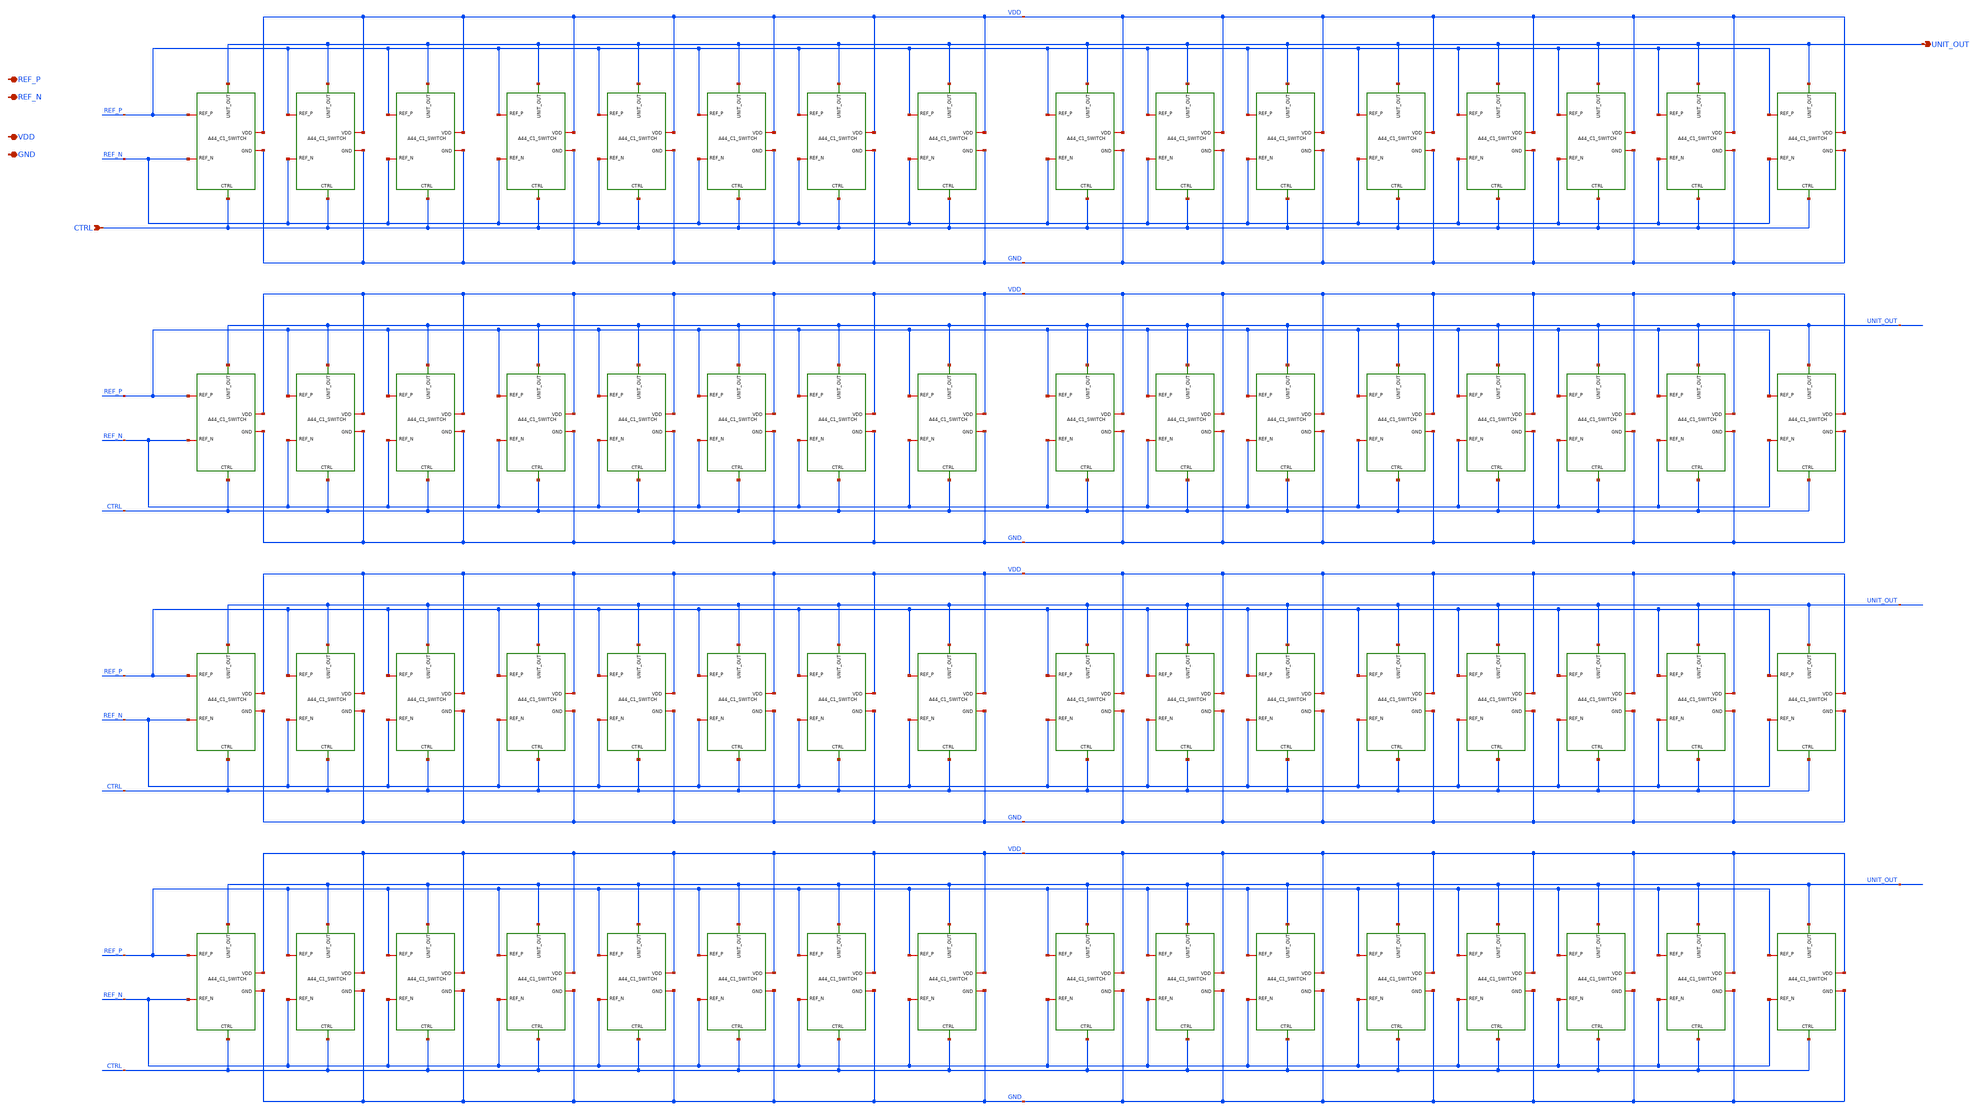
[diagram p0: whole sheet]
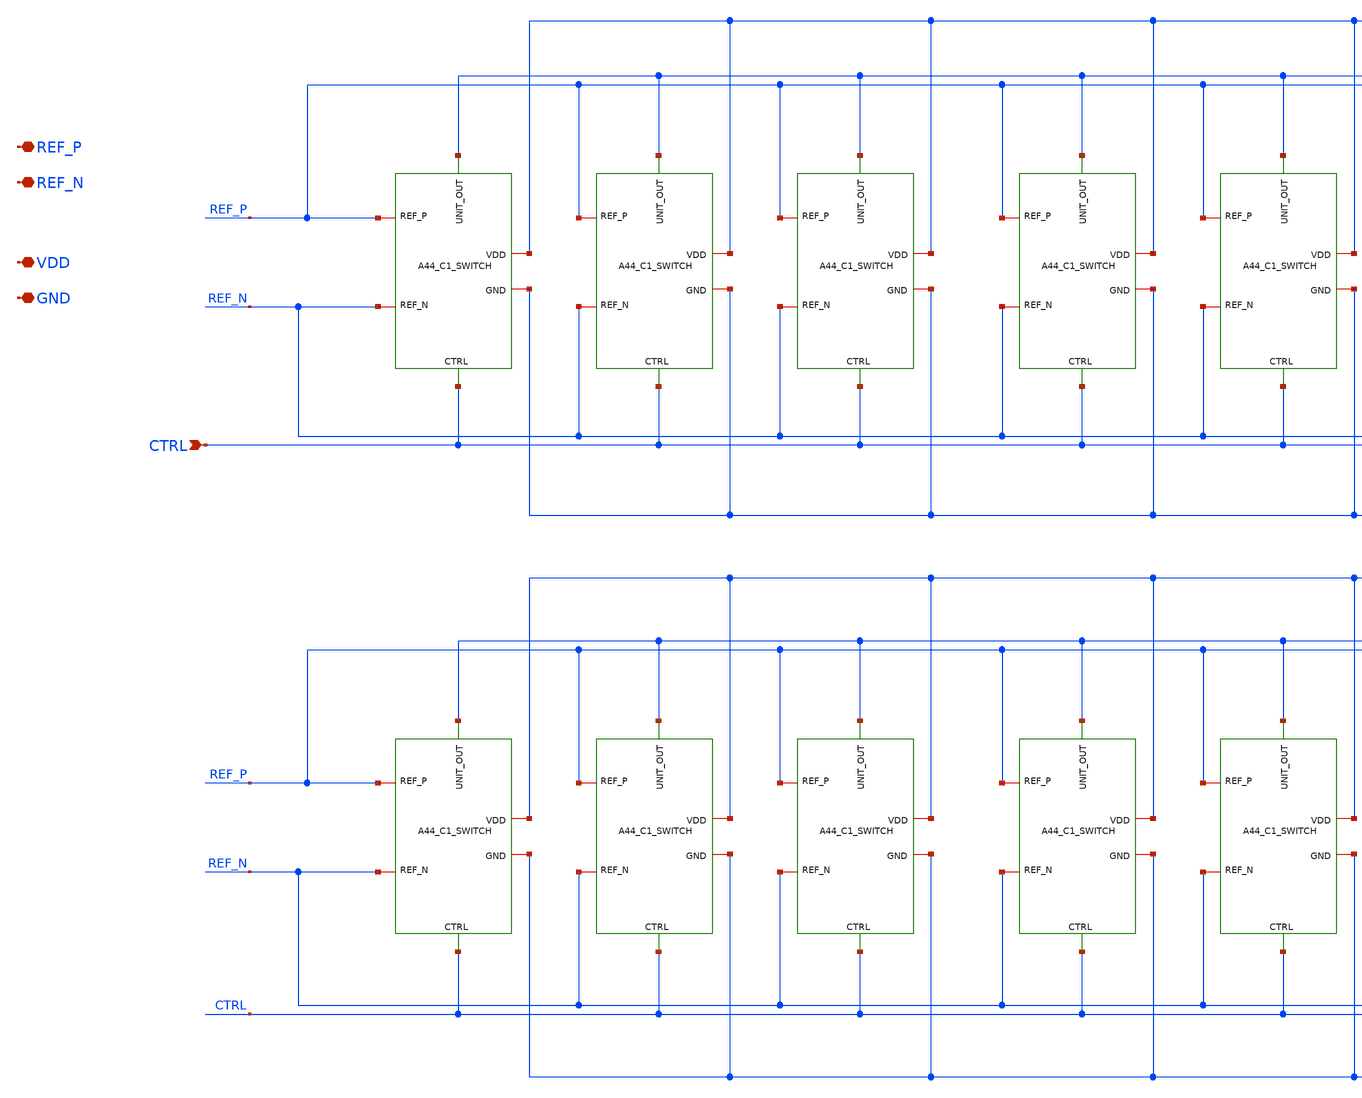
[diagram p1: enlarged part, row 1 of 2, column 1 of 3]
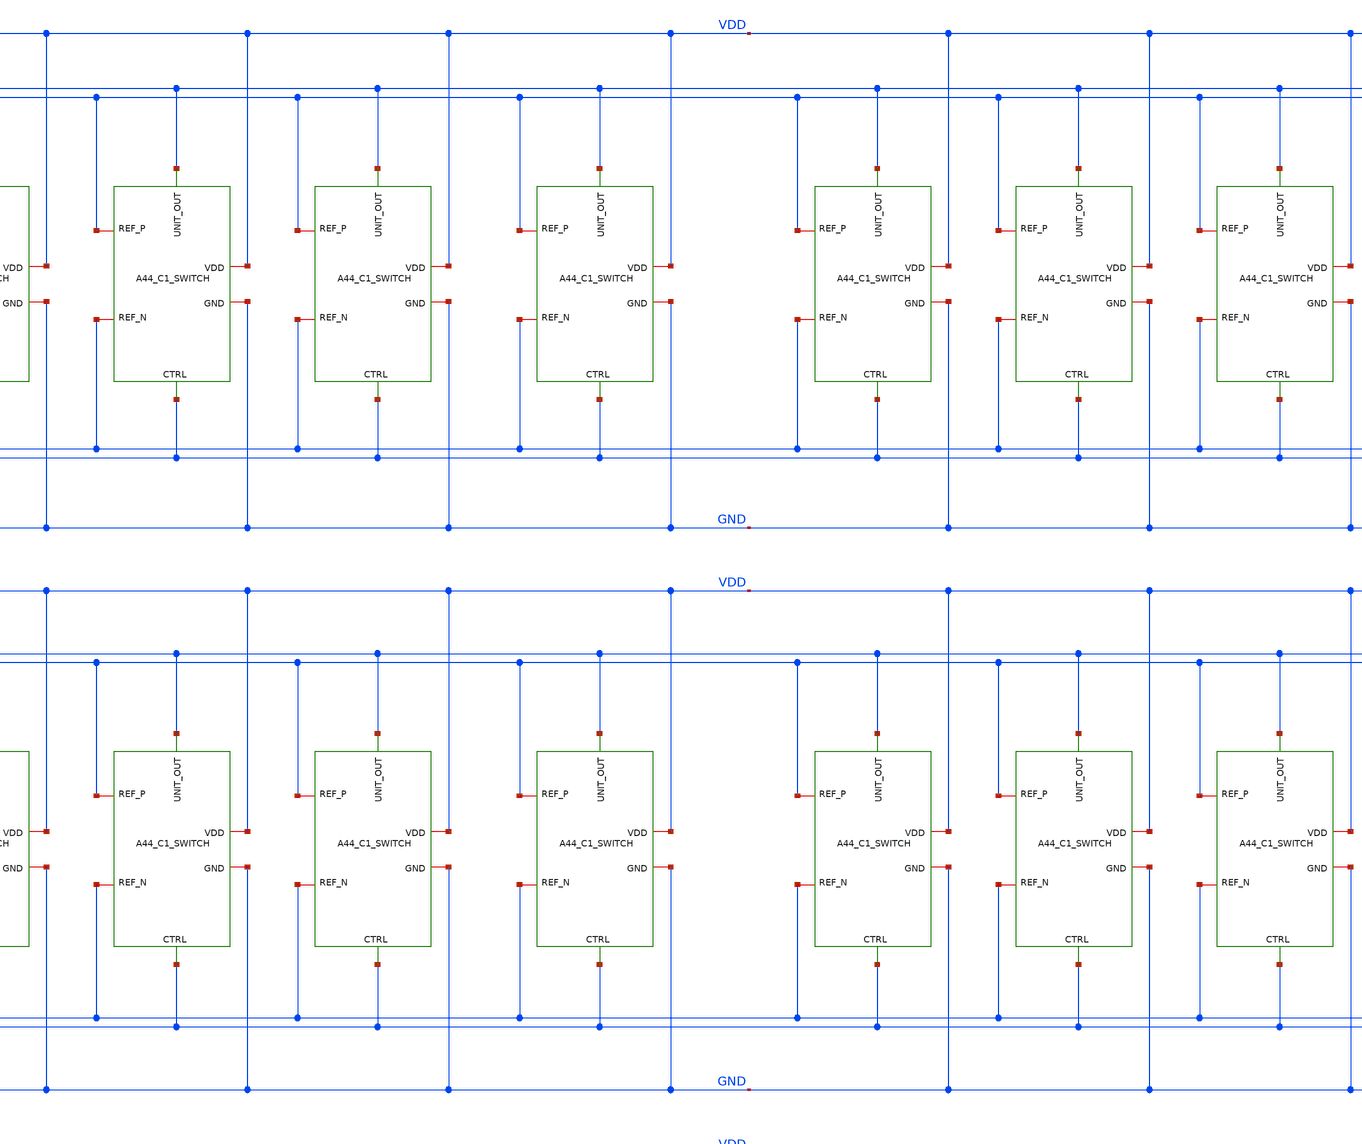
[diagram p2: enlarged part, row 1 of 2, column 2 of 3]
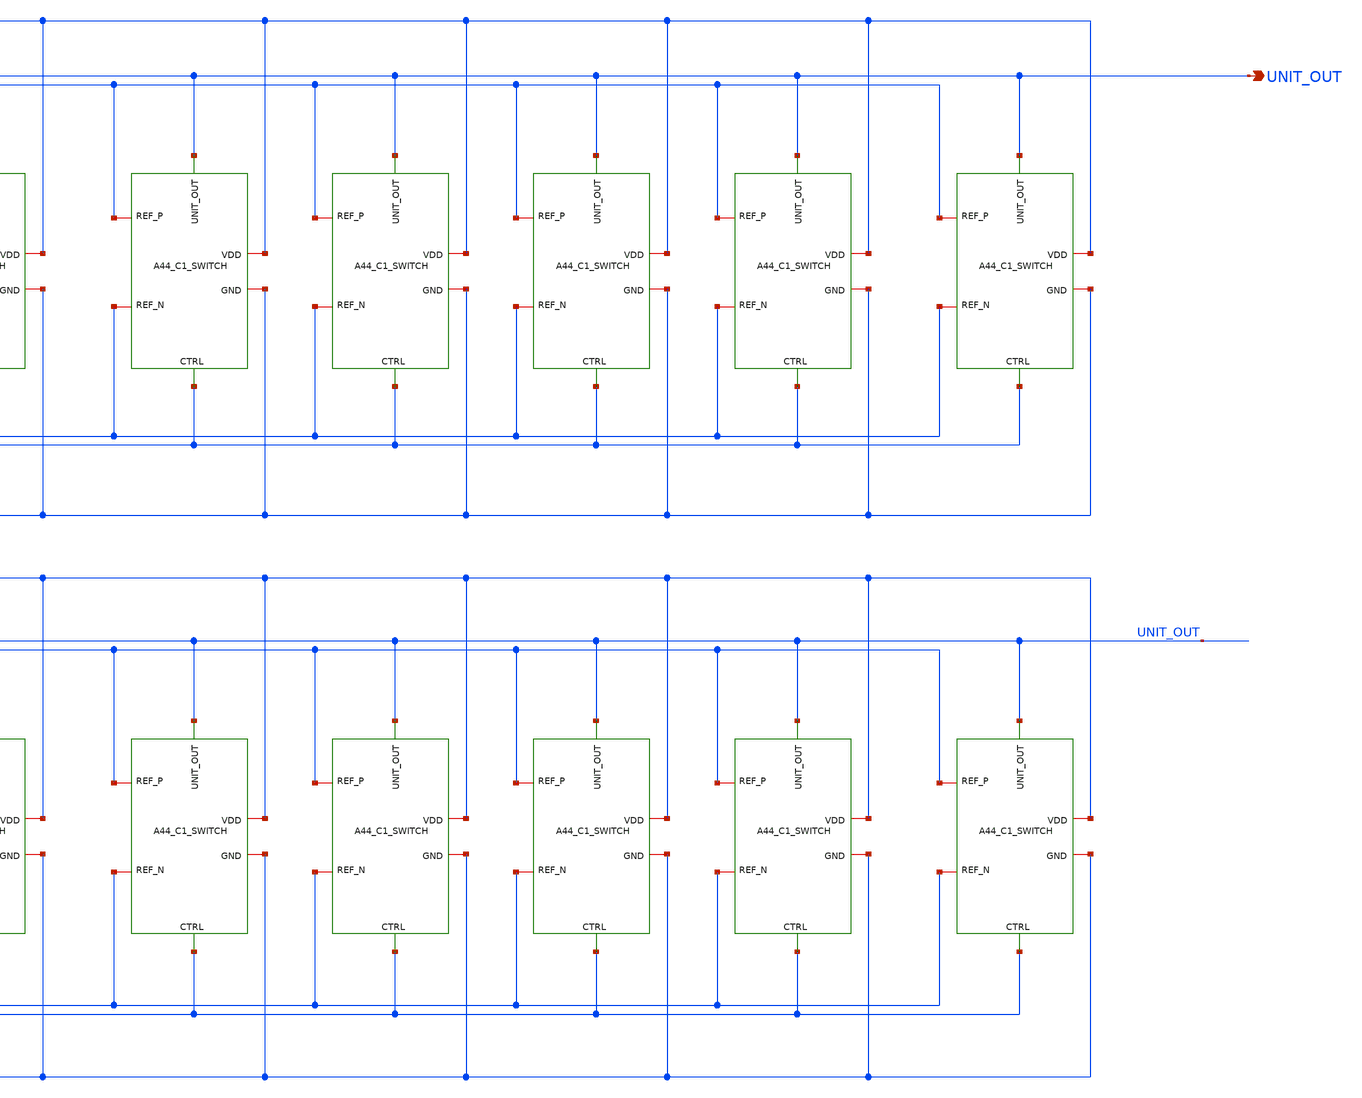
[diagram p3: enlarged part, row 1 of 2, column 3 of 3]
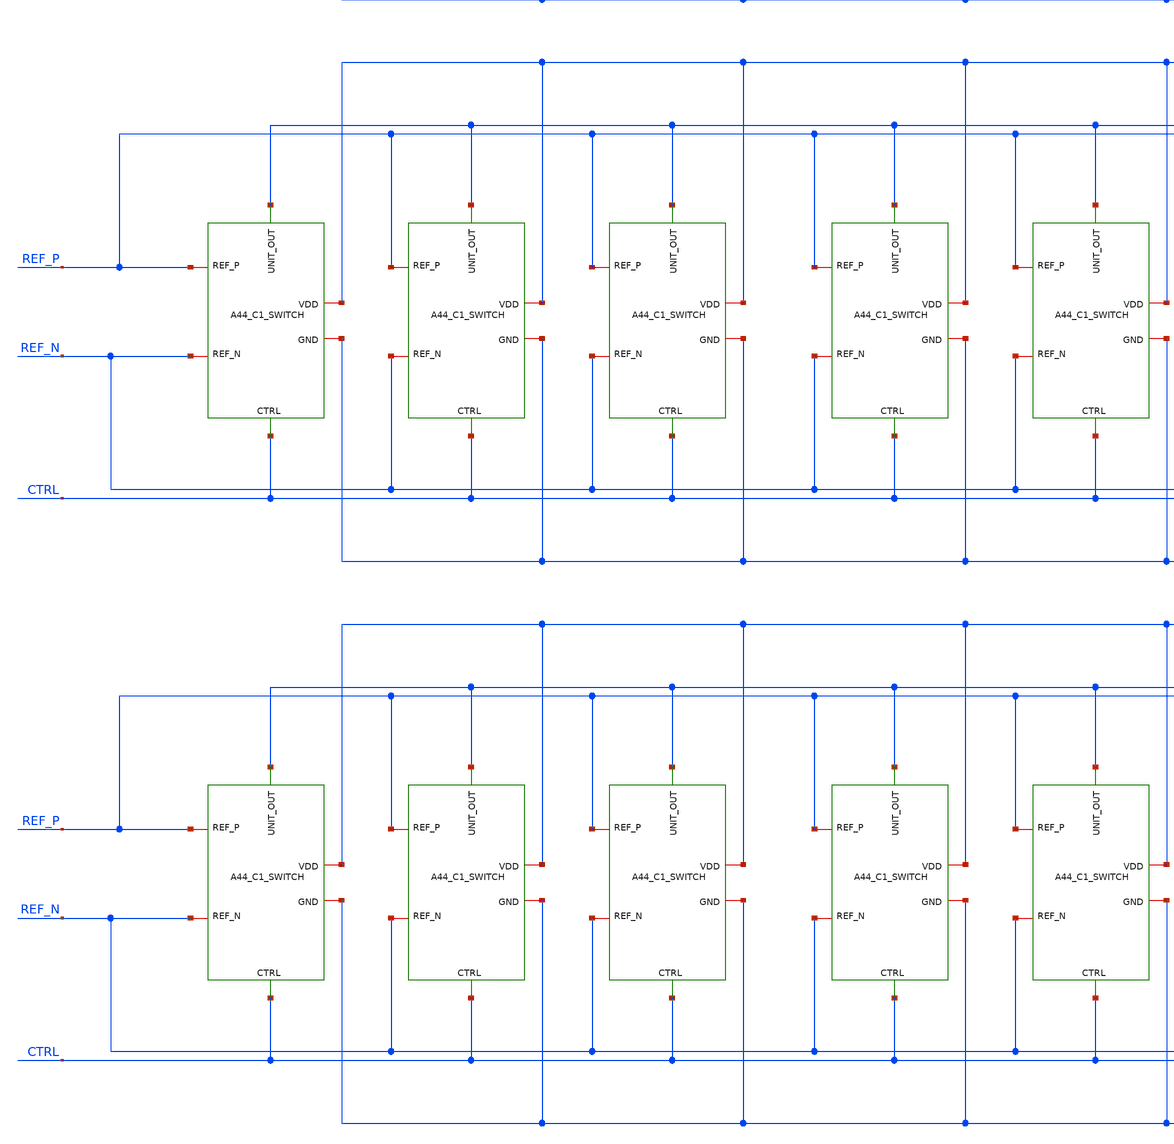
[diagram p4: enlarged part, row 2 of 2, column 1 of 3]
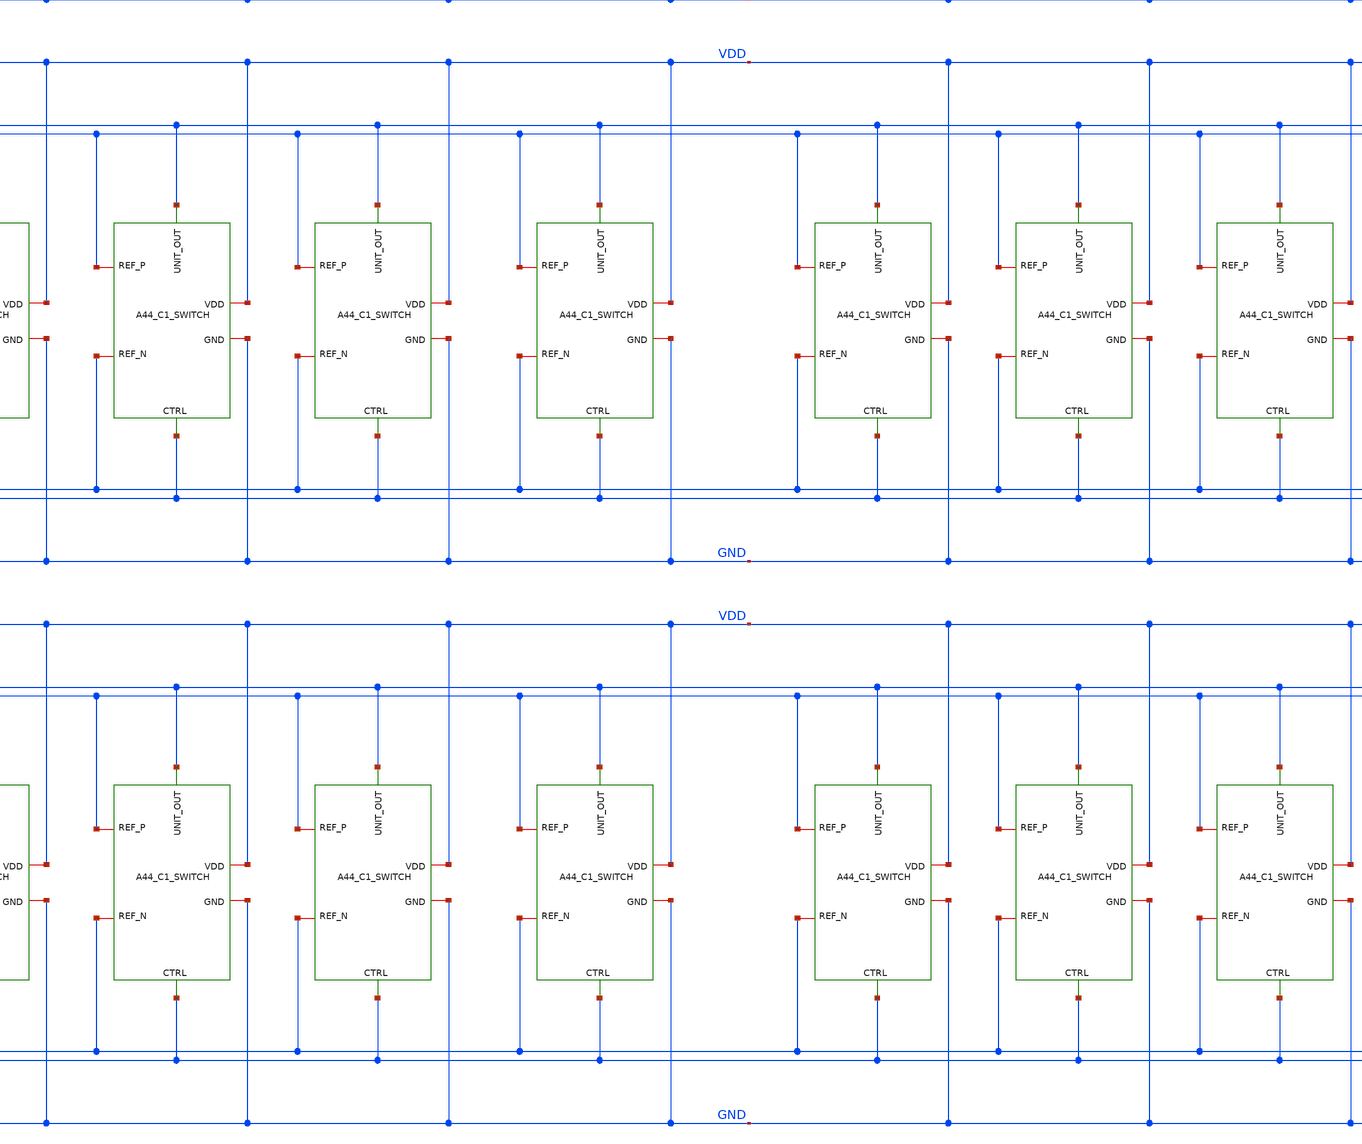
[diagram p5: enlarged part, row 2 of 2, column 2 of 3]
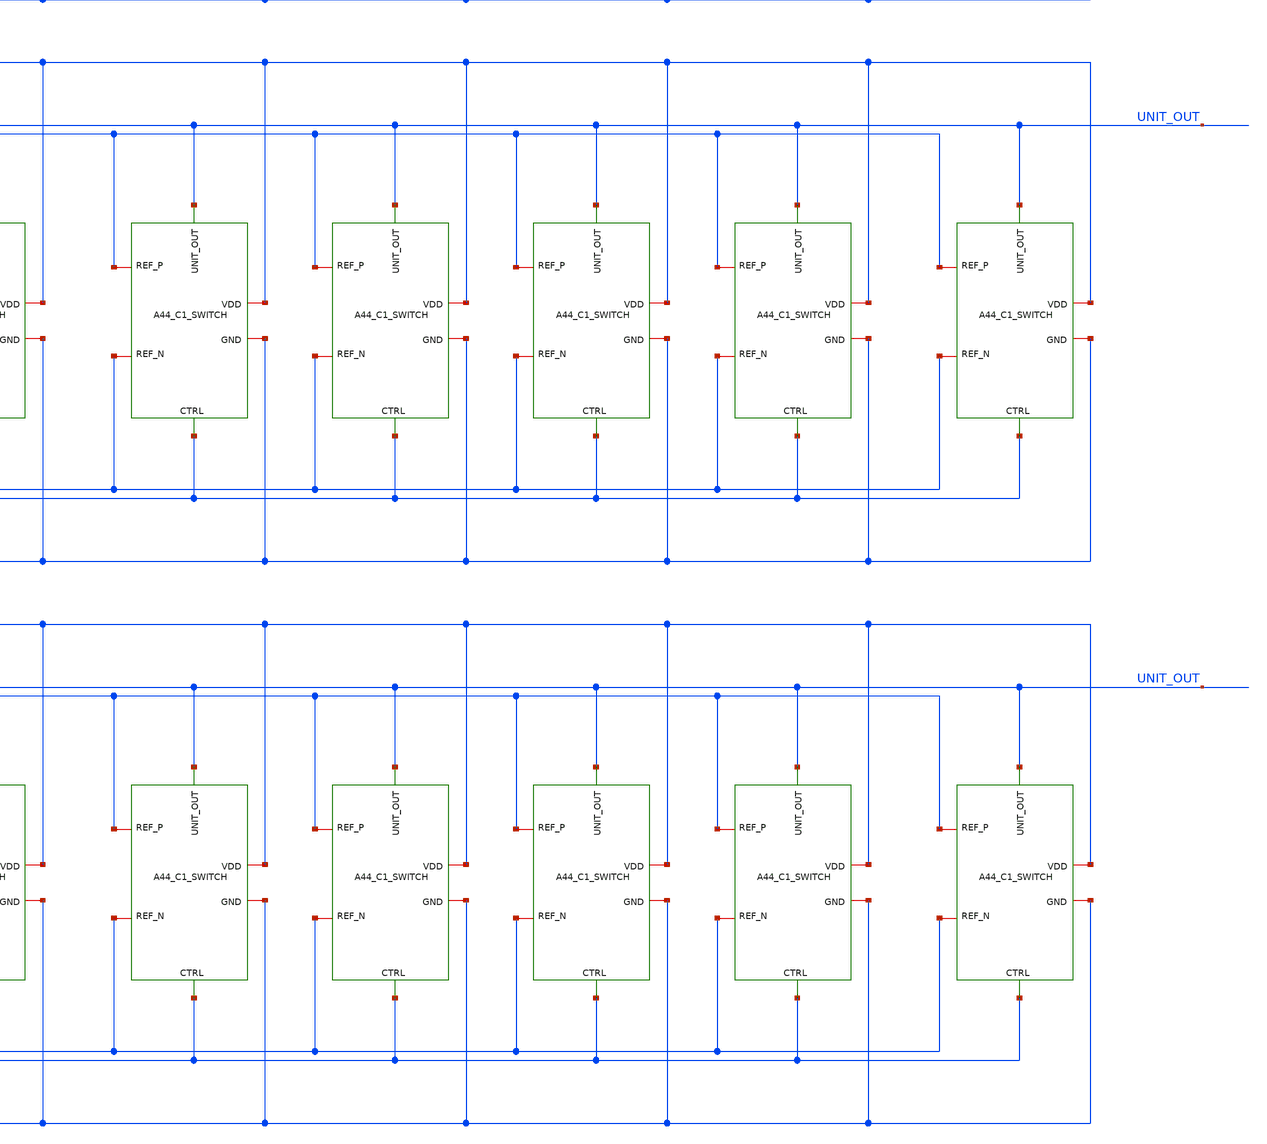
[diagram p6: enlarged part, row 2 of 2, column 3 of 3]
** sch_path: verification/a44_w5p29_trans_driver/01_CURRENT_CIRCUIT_FILES/xschem/A44_C64_SWITCH.sch
**.subckt A44_C64_SWITCH REF_N REF_P VDD GND CTRL UNIT_OUT
*.iopin REF_N
*.iopin REF_P
*.iopin VDD
*.iopin GND
*.ipin CTRL
*.opin UNIT_OUT
x1 REF_N REF_P VDD GND UNIT_OUT CTRL A44_C1_SWITCH
x2 REF_N REF_P VDD GND UNIT_OUT CTRL A44_C1_SWITCH
x3 REF_N REF_P VDD GND UNIT_OUT CTRL A44_C1_SWITCH
x4 REF_N REF_P VDD GND UNIT_OUT CTRL A44_C1_SWITCH
x5 REF_N REF_P VDD GND UNIT_OUT CTRL A44_C1_SWITCH
x6 REF_N REF_P VDD GND UNIT_OUT CTRL A44_C1_SWITCH
x7 REF_N REF_P VDD GND UNIT_OUT CTRL A44_C1_SWITCH
x8 REF_N REF_P VDD GND UNIT_OUT CTRL A44_C1_SWITCH
x9 REF_N REF_P VDD GND UNIT_OUT CTRL A44_C1_SWITCH
x10 REF_N REF_P VDD GND UNIT_OUT CTRL A44_C1_SWITCH
x11 REF_N REF_P VDD GND UNIT_OUT CTRL A44_C1_SWITCH
x12 REF_N REF_P VDD GND UNIT_OUT CTRL A44_C1_SWITCH
x13 REF_N REF_P VDD GND UNIT_OUT CTRL A44_C1_SWITCH
x14 REF_N REF_P VDD GND UNIT_OUT CTRL A44_C1_SWITCH
x15 REF_N REF_P VDD GND UNIT_OUT CTRL A44_C1_SWITCH
x16 REF_N REF_P VDD GND UNIT_OUT CTRL A44_C1_SWITCH
x17 REF_N REF_P VDD GND UNIT_OUT CTRL A44_C1_SWITCH
x18 REF_N REF_P VDD GND UNIT_OUT CTRL A44_C1_SWITCH
x19 REF_N REF_P VDD GND UNIT_OUT CTRL A44_C1_SWITCH
x20 REF_N REF_P VDD GND UNIT_OUT CTRL A44_C1_SWITCH
x21 REF_N REF_P VDD GND UNIT_OUT CTRL A44_C1_SWITCH
x22 REF_N REF_P VDD GND UNIT_OUT CTRL A44_C1_SWITCH
x23 REF_N REF_P VDD GND UNIT_OUT CTRL A44_C1_SWITCH
x24 REF_N REF_P VDD GND UNIT_OUT CTRL A44_C1_SWITCH
x25 REF_N REF_P VDD GND UNIT_OUT CTRL A44_C1_SWITCH
x26 REF_N REF_P VDD GND UNIT_OUT CTRL A44_C1_SWITCH
x27 REF_N REF_P VDD GND UNIT_OUT CTRL A44_C1_SWITCH
x28 REF_N REF_P VDD GND UNIT_OUT CTRL A44_C1_SWITCH
x29 REF_N REF_P VDD GND UNIT_OUT CTRL A44_C1_SWITCH
x30 REF_N REF_P VDD GND UNIT_OUT CTRL A44_C1_SWITCH
x31 REF_N REF_P VDD GND UNIT_OUT CTRL A44_C1_SWITCH
x32 REF_N REF_P VDD GND UNIT_OUT CTRL A44_C1_SWITCH
x33 REF_N REF_P VDD GND UNIT_OUT CTRL A44_C1_SWITCH
x34 REF_N REF_P VDD GND UNIT_OUT CTRL A44_C1_SWITCH
x35 REF_N REF_P VDD GND UNIT_OUT CTRL A44_C1_SWITCH
x36 REF_N REF_P VDD GND UNIT_OUT CTRL A44_C1_SWITCH
x37 REF_N REF_P VDD GND UNIT_OUT CTRL A44_C1_SWITCH
x38 REF_N REF_P VDD GND UNIT_OUT CTRL A44_C1_SWITCH
x39 REF_N REF_P VDD GND UNIT_OUT CTRL A44_C1_SWITCH
x40 REF_N REF_P VDD GND UNIT_OUT CTRL A44_C1_SWITCH
x41 REF_N REF_P VDD GND UNIT_OUT CTRL A44_C1_SWITCH
x42 REF_N REF_P VDD GND UNIT_OUT CTRL A44_C1_SWITCH
x43 REF_N REF_P VDD GND UNIT_OUT CTRL A44_C1_SWITCH
x44 REF_N REF_P VDD GND UNIT_OUT CTRL A44_C1_SWITCH
x45 REF_N REF_P VDD GND UNIT_OUT CTRL A44_C1_SWITCH
x46 REF_N REF_P VDD GND UNIT_OUT CTRL A44_C1_SWITCH
x47 REF_N REF_P VDD GND UNIT_OUT CTRL A44_C1_SWITCH
x48 REF_N REF_P VDD GND UNIT_OUT CTRL A44_C1_SWITCH
x49 REF_N REF_P VDD GND UNIT_OUT CTRL A44_C1_SWITCH
x50 REF_N REF_P VDD GND UNIT_OUT CTRL A44_C1_SWITCH
x51 REF_N REF_P VDD GND UNIT_OUT CTRL A44_C1_SWITCH
x52 REF_N REF_P VDD GND UNIT_OUT CTRL A44_C1_SWITCH
x53 REF_N REF_P VDD GND UNIT_OUT CTRL A44_C1_SWITCH
x54 REF_N REF_P VDD GND UNIT_OUT CTRL A44_C1_SWITCH
x55 REF_N REF_P VDD GND UNIT_OUT CTRL A44_C1_SWITCH
x56 REF_N REF_P VDD GND UNIT_OUT CTRL A44_C1_SWITCH
x57 REF_N REF_P VDD GND UNIT_OUT CTRL A44_C1_SWITCH
x58 REF_N REF_P VDD GND UNIT_OUT CTRL A44_C1_SWITCH
x59 REF_N REF_P VDD GND UNIT_OUT CTRL A44_C1_SWITCH
x60 REF_N REF_P VDD GND UNIT_OUT CTRL A44_C1_SWITCH
x61 REF_N REF_P VDD GND UNIT_OUT CTRL A44_C1_SWITCH
x62 REF_N REF_P VDD GND UNIT_OUT CTRL A44_C1_SWITCH
x63 REF_N REF_P VDD GND UNIT_OUT CTRL A44_C1_SWITCH
x64 REF_N REF_P VDD GND UNIT_OUT CTRL A44_C1_SWITCH
**.ends

* expanding   symbol:  A44_C1_SWITCH.sym # of pins=6
** sym_path: verification/a44_w5p29_trans_driver/01_CURRENT_CIRCUIT_FILES/xschem/A44_C1_SWITCH.sym
** sch_path: verification/a44_w5p29_trans_driver/01_CURRENT_CIRCUIT_FILES/xschem/A44_C1_SWITCH.sch
.subckt A44_C1_SWITCH REF_N REF_P VDD GND UNIT_OUT CTRL
*.iopin REF_N
*.iopin REF_P
*.iopin VDD
*.iopin GND
*.ipin CTRL
*.opin UNIT_OUT
x1 REF_P REF_N CTRL V_BOT VDD GND A44_CAP_SWITCH
XC1 UNIT_OUT V_BOT cap_mim_2f0_m4m5_noshield c_width=6.855e-6 c_length=6.855e-6 m=18
.ends


* expanding   symbol:  A44_CAP_SWITCH.sym # of pins=6
** sym_path: verification/a44_w5p29_trans_driver/01_CURRENT_CIRCUIT_FILES/xschem/A44_CAP_SWITCH.sym
** sch_path: verification/a44_w5p29_trans_driver/01_CURRENT_CIRCUIT_FILES/xschem/A44_CAP_SWITCH.sch
.subckt A44_CAP_SWITCH VREFP VREFN CTRL CAP_BOTTOM VDD GND
*.iopin VREFP
*.iopin VREFN
*.ipin CTRL
*.opin CAP_BOTTOM
*.iopin VDD
*.iopin GND
XCAP_REFN_SWITCH_NMOS CAP_BOTTOM CTRL VREFN GND nfet_03v3 L=0.28u W=1.56u nf=1 ad='int((nf+1)/2) * W/nf * 0.18u'
+ as='int((nf+2)/2) * W/nf * 0.18u' pd='2*int((nf+1)/2) * (W/nf + 0.18u)' ps='2*int((nf+2)/2) * (W/nf + 0.18u)'
+ nrd='0.18u / W' nrs='0.18u / W' sa=0 sb=0 sd=0 m=18
XCAP_REFP_SWITCH_PMOS CAP_BOTTOM CTRL VREFP VDD pfet_03v3 L=0.28u W=1.56u nf=1 ad='int((nf+1)/2) * W/nf * 0.18u'
+ as='int((nf+2)/2) * W/nf * 0.18u' pd='2*int((nf+1)/2) * (W/nf + 0.18u)' ps='2*int((nf+2)/2) * (W/nf + 0.18u)'
+ nrd='0.18u / W' nrs='0.18u / W' sa=0 sb=0 sd=0 m=18
.ends

.end
